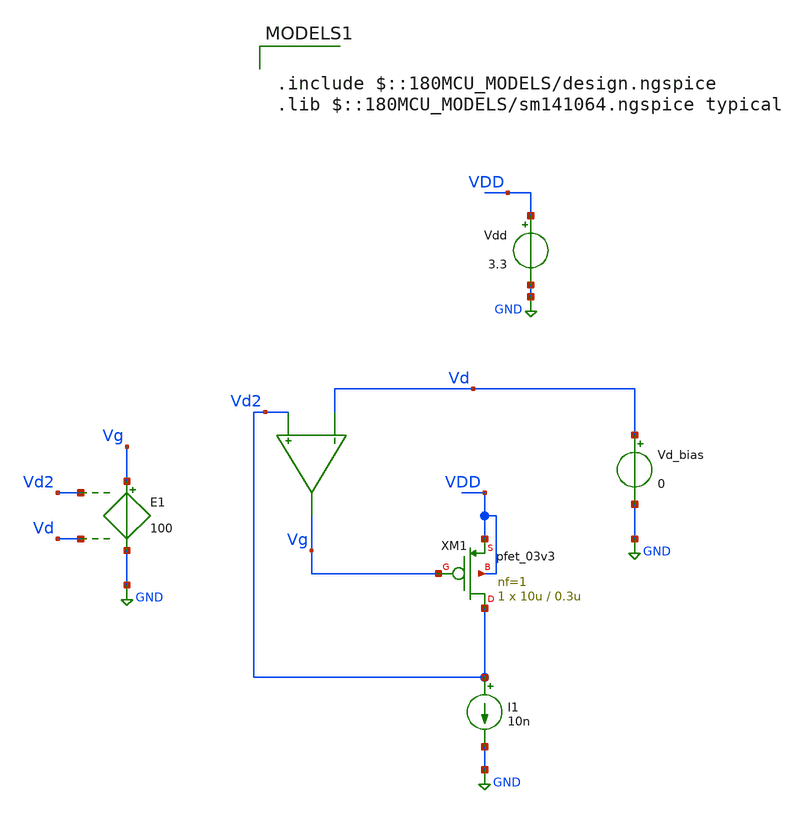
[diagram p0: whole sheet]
** sch_path: legacy/Examples/GF180MCU/xschem/Extraction/pmos_sigma_ext.sch
**.subckt pmos_sigma_ext
I1 Vd2 GND 10n
Vd_bias Vd GND 0
Vdd VDD GND 3.3
E1 Vg GND Vd2 Vd 100
XM1 Vd2 Vg VDD VDD pfet_03v3 L=0.3u W=10u nf=1 ad='int((nf+1)/2) * W/nf * 0.18u' as='int((nf+2)/2) * W/nf * 0.18u'
+ pd='2*int((nf+1)/2) * (W/nf + 0.18u)' ps='2*int((nf+2)/2) * (W/nf + 0.18u)' nrd='0.18u / W' nrs='0.18u / W'
+ sa=0 sb=0 sd=0 m=1
**** begin user architecture code


.option gmin=1e-18


.control
save all

dc Vd_bias  0 -4 -25.9m

let vd_interp = -3.3/3
let sigma = -deriv(V(vg))/deriv(V(vd))
save sigma

echo
echo
echo


echo Sigma @ VD=$&vd_interp:
meas dc sigma_value FIND sigma WHEN V(vd)=vd_interp

echo
echo
echo
write pmos_sigma_ext.raw

.endc





.include $::180MCU_MODELS/design.ngspice
.lib $::180MCU_MODELS/sm141064.ngspice typical

**** end user architecture code
**.ends
.GLOBAL GND
.end
